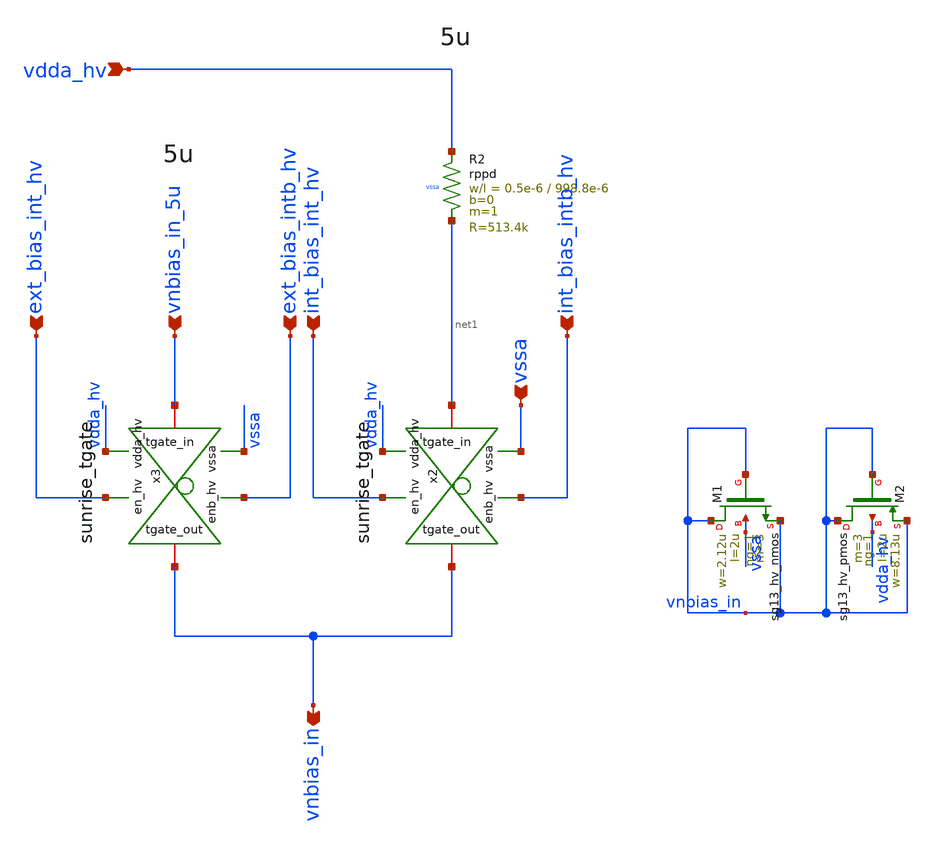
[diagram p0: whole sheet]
** sch_path: Schematics_Layout/sunrise_int_ext_bias/sunrise_int_ext_bias.sch
**.subckt sunrise_int_ext_bias vnbias_in_5u vdda_hv ext_bias_intb_hv ext_bias_int_hv
*+ int_bias_intb_hv int_bias_int_hv vnbias_in vssa
*.ipin vnbias_in_5u
*.ipin vdda_hv
*.ipin ext_bias_intb_hv
*.ipin ext_bias_int_hv
*.ipin int_bias_intb_hv
*.ipin int_bias_int_hv
*.opin vnbias_in
*.ipin vssa
XR2 vdda_hv net1 vssa rppd w=0.5e-6 l=998.8e-6 m=1 b=0 mm_ok=1
x2 vdda_hv vssa int_bias_int_hv net1 vnbias_in int_bias_intb_hv sunrise_tgate
x3 vdda_hv vssa ext_bias_int_hv vnbias_in_5u vnbias_in ext_bias_intb_hv sunrise_tgate
XM1 vnbias_in vnbias_in vnbias_in vssa sg13_hv_nmos w=2.12u l=2u ng=1 m=3 mm_ok=1
XM2 vnbias_in vnbias_in vnbias_in vdda_hv sg13_hv_pmos w=8.13u l=2u ng=1 m=3 mm_ok=1
**.ends
.end
